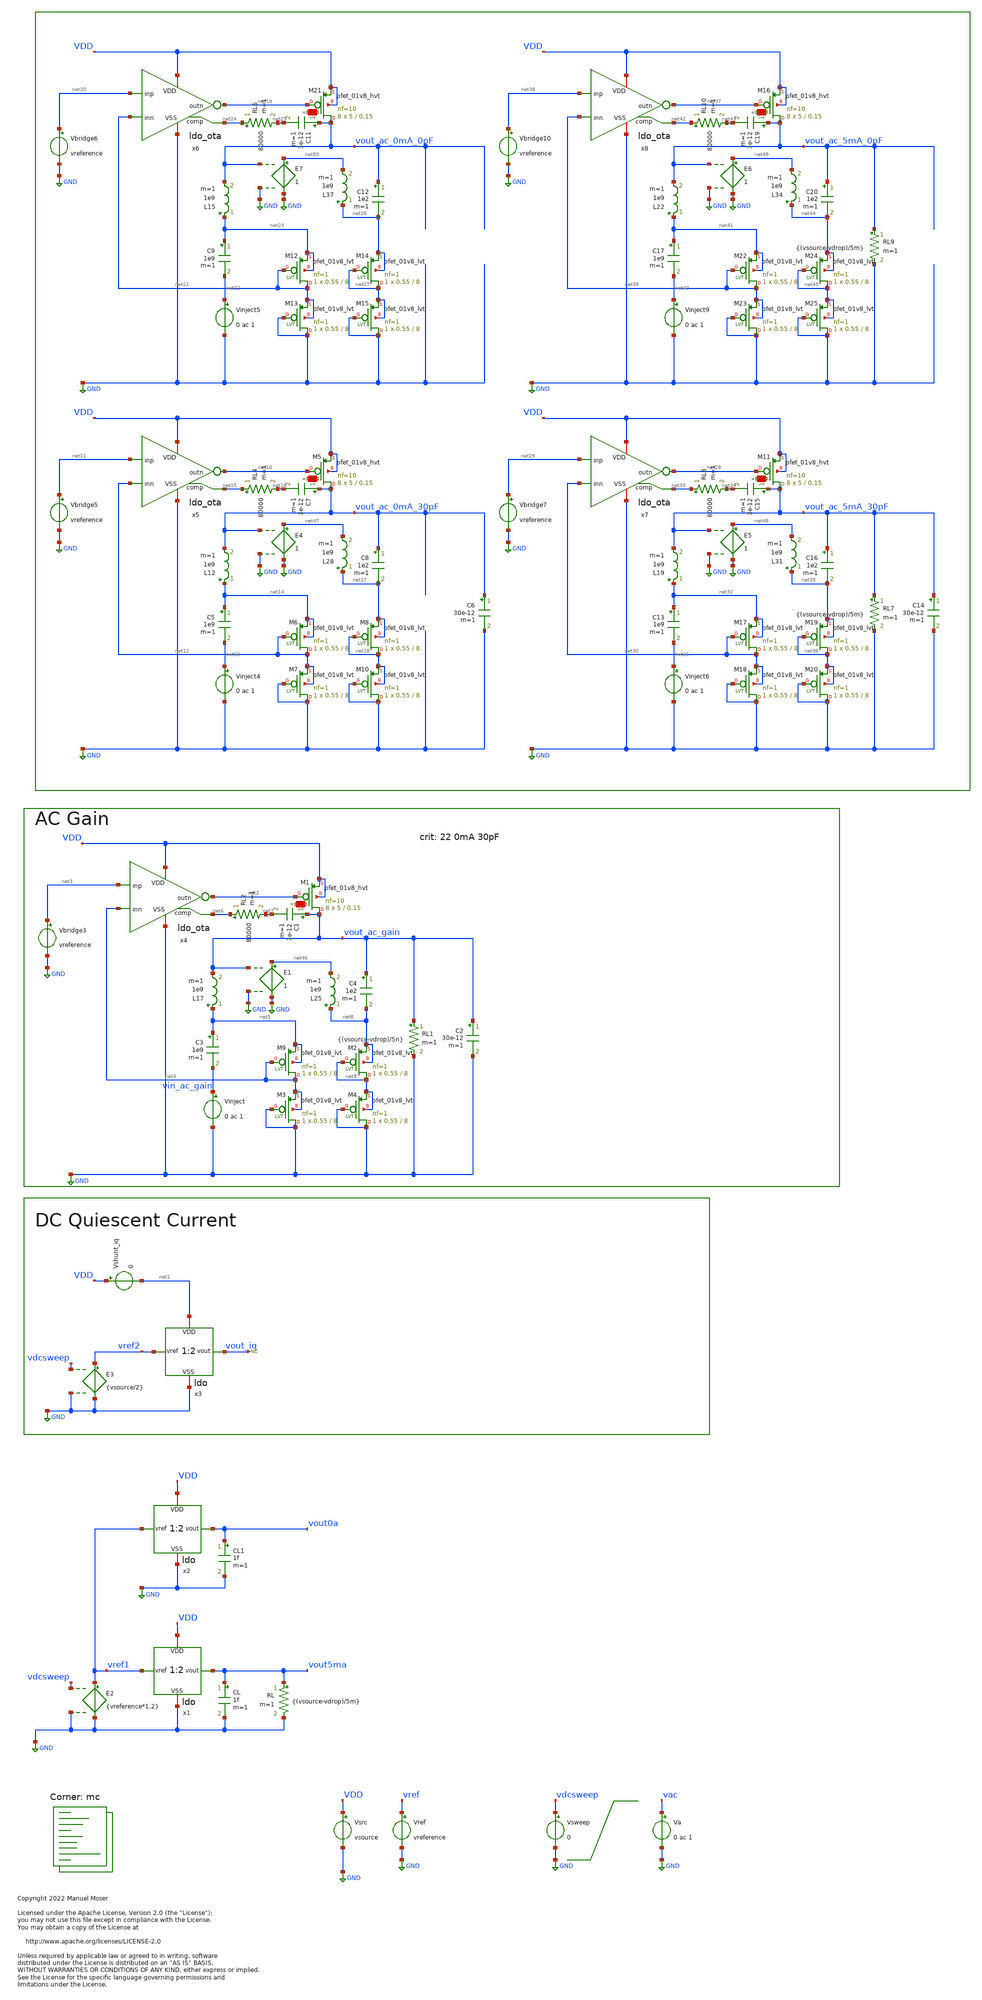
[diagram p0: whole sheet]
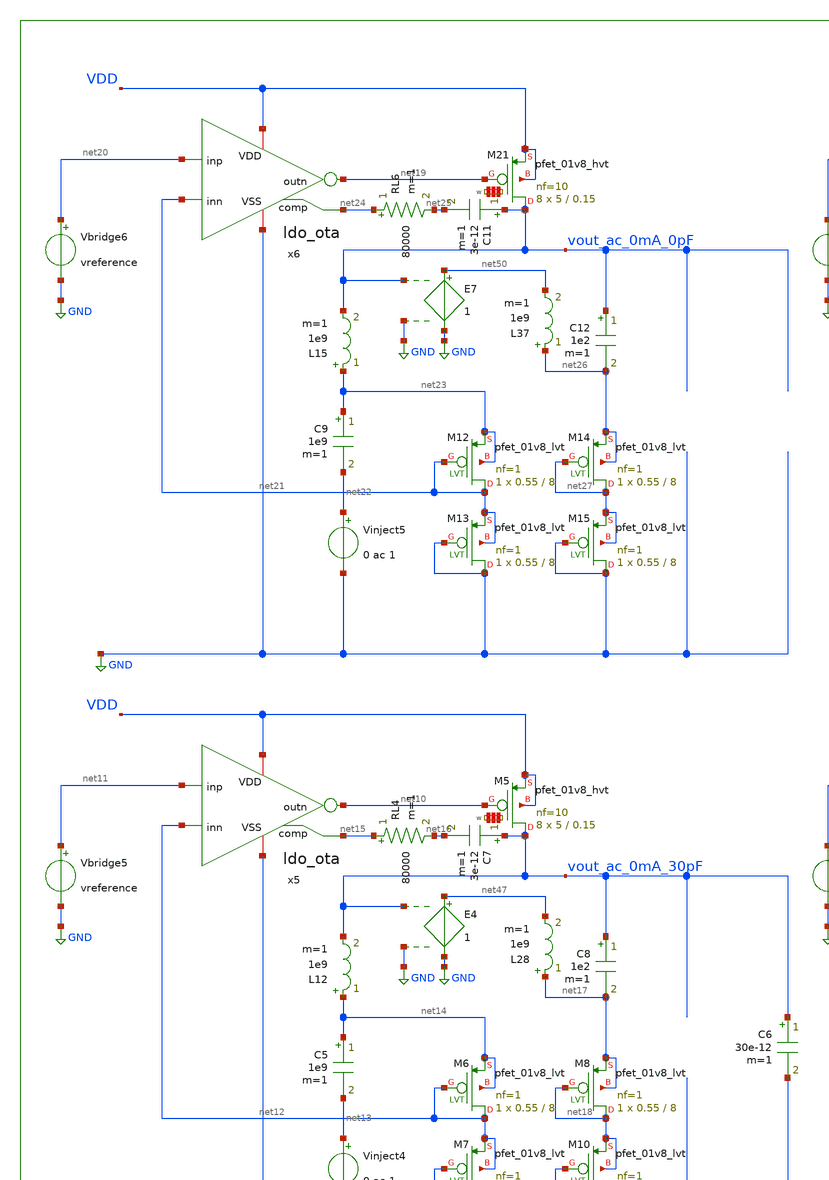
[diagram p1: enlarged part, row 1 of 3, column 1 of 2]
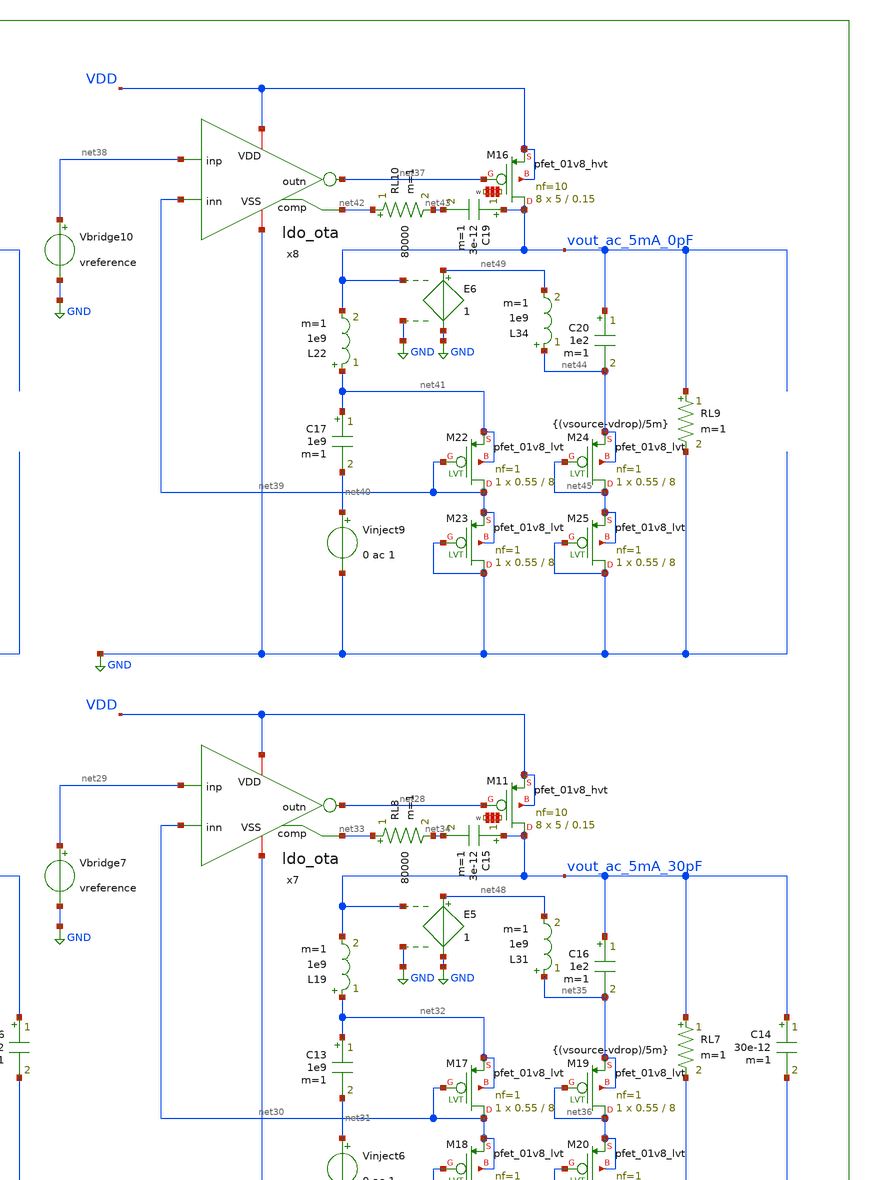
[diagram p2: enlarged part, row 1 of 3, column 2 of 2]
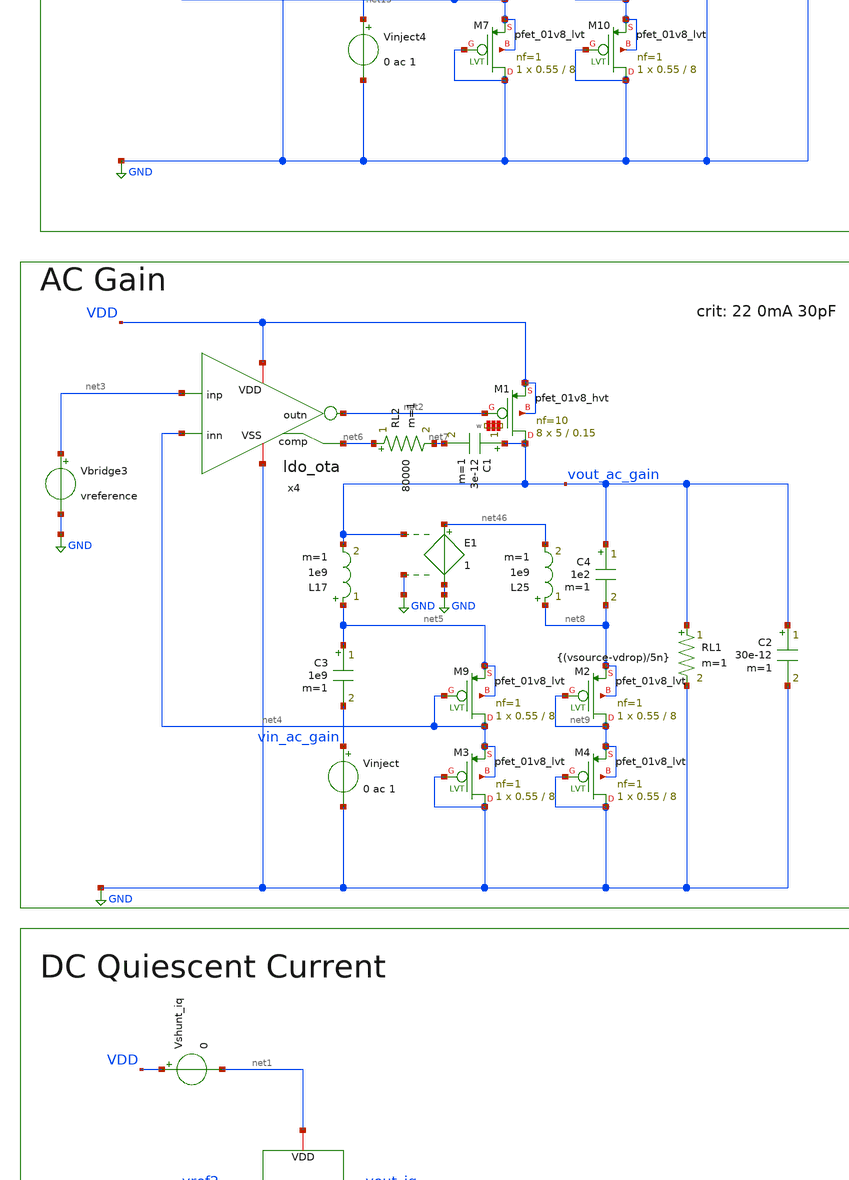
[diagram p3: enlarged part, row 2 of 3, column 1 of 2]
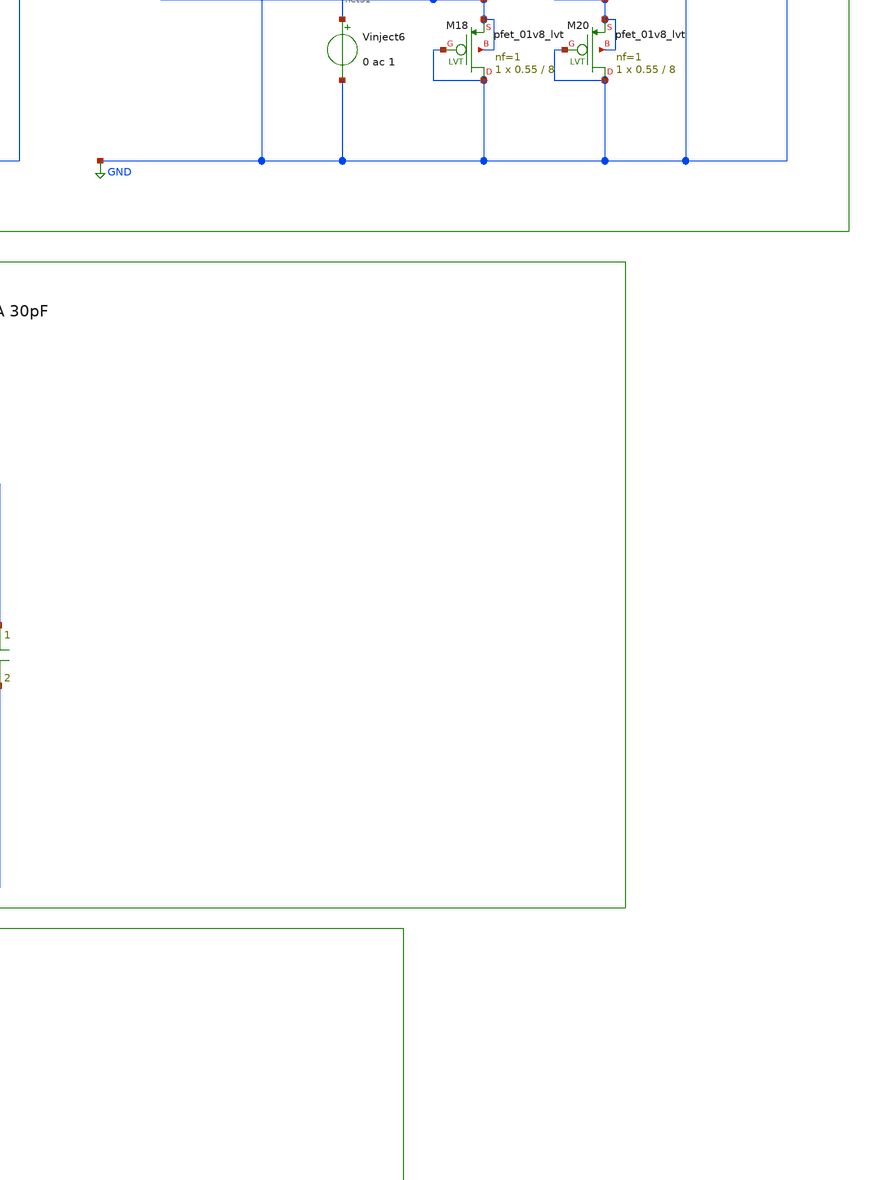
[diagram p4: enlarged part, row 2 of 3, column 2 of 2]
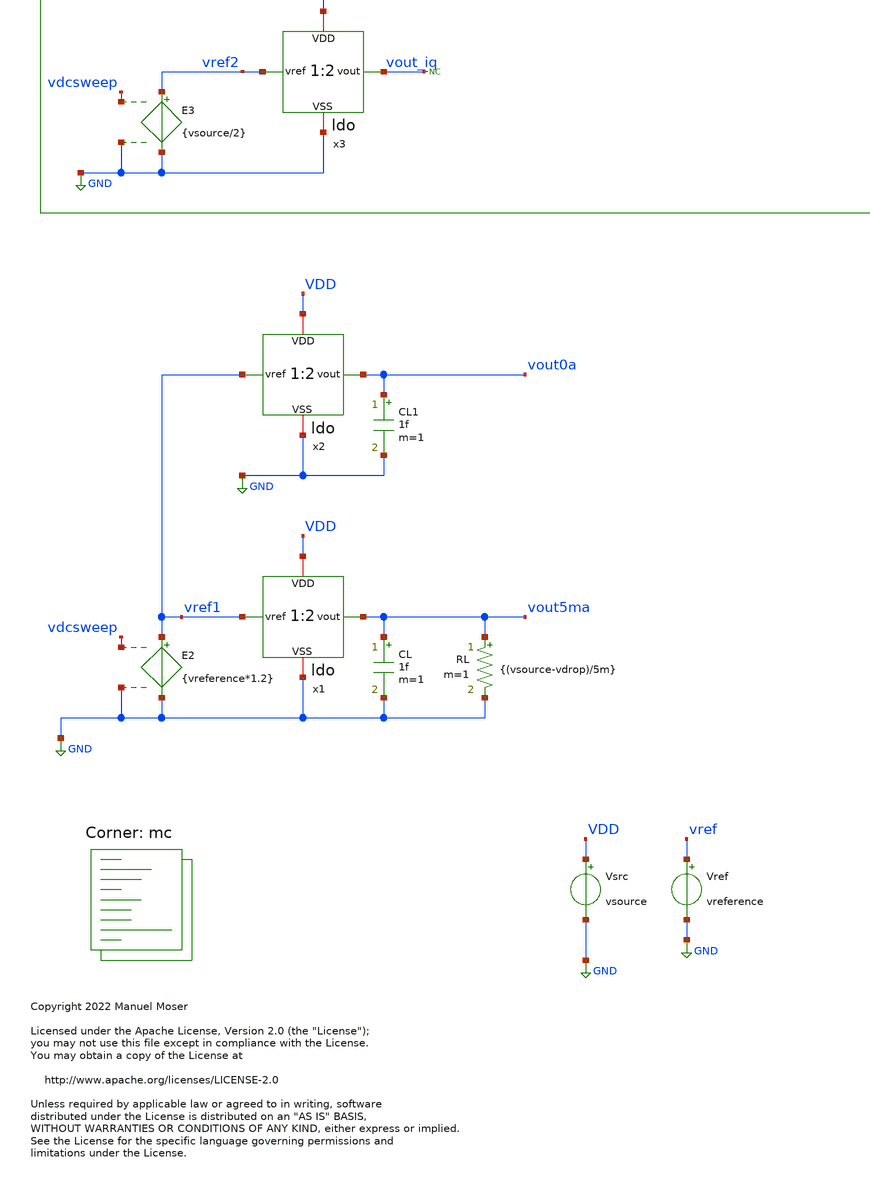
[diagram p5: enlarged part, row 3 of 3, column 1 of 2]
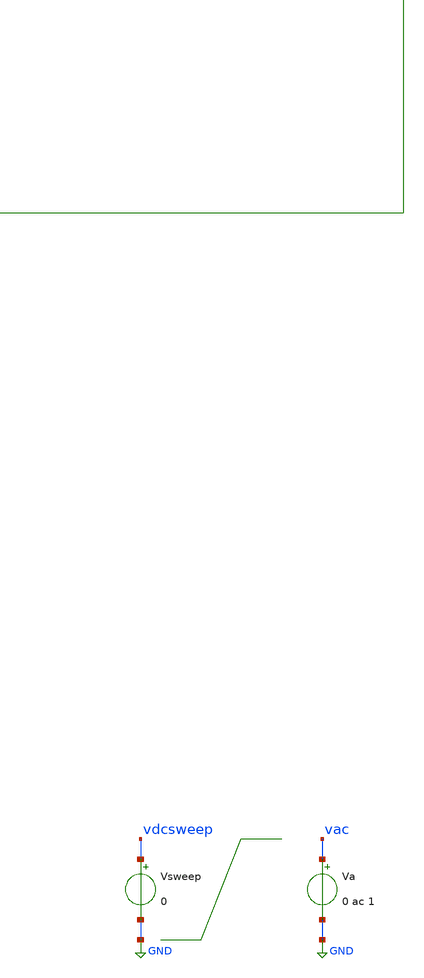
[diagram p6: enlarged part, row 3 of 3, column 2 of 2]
** sch_path: xschem/ldo_tb.sch
* Copyright 2022 Manuel Moser
* Licensed under the Apache License, Version 2.0 (the "License");
**.subckt ldo_tb
Vref vref GND vreference
Vsrc VDD GND vsource
Va vac GND 0 ac 1
CL vout5ma GND 1f m=1
RL vout5ma GND {(vsource-vdrop)/5m} m=1
x1 VDD vref1 vout5ma GND ldo
CL1 vout0a GND 1f m=1
x2 VDD vref1 vout0a GND ldo
Vsweep vdcsweep GND 0
E2 vref1 GND vdcsweep GND {vreference*1.2}
x3 net1 vref2 vout_iq GND ldo
Vshunt_iq VDD net1 0
E3 vref2 GND vdcsweep GND {vsource/2}
* noconn vout_iq
x4 VDD net3 net2 net4 GND net6 ldo_ota
L17 net5 vout_ac_gain 1e9 m=1
C3 net5 vin_ac_gain 1e9 m=1
Vinject vin_ac_gain GND 0 ac 1
Vbridge3 net3 GND vreference
RL1 vout_ac_gain GND {(vsource-vdrop)/5n} m=1
C2 vout_ac_gain GND 30e-12 m=1
C1 vout_ac_gain net7 3e-12 m=1
RL2 net6 net7 80000 m=1
XM9 net4 net4 net5 net5 sky130_fd_pr__pfet_01v8_lvt L=8 W=0.55 nf=1 ad='int((nf+1)/2) * W/nf * 0.29'
+ as='int((nf+2)/2) * W/nf * 0.29' pd='2*int((nf+1)/2) * (W/nf + 0.29)' ps='2*int((nf+2)/2) * (W/nf + 0.29)'
+ nrd='0.29 / W' nrs='0.29 / W' sa=0 sb=0 sd=0 mult=1 m=1
XM3 GND GND net4 net4 sky130_fd_pr__pfet_01v8_lvt L=8 W=0.55 nf=1 ad='int((nf+1)/2) * W/nf * 0.29' as='int((nf+2)/2) * W/nf * 0.29'
+ pd='2*int((nf+1)/2) * (W/nf + 0.29)' ps='2*int((nf+2)/2) * (W/nf + 0.29)' nrd='0.29 / W' nrs='0.29 / W'
+ sa=0 sb=0 sd=0 mult=1 m=1
XM2 net9 net9 net8 net8 sky130_fd_pr__pfet_01v8_lvt L=8 W=0.55 nf=1 ad='int((nf+1)/2) * W/nf * 0.29'
+ as='int((nf+2)/2) * W/nf * 0.29' pd='2*int((nf+1)/2) * (W/nf + 0.29)' ps='2*int((nf+2)/2) * (W/nf + 0.29)'
+ nrd='0.29 / W' nrs='0.29 / W' sa=0 sb=0 sd=0 mult=1 m=1
XM4 GND GND net9 net9 sky130_fd_pr__pfet_01v8_lvt L=8 W=0.55 nf=1 ad='int((nf+1)/2) * W/nf * 0.29' as='int((nf+2)/2) * W/nf * 0.29'
+ pd='2*int((nf+1)/2) * (W/nf + 0.29)' ps='2*int((nf+2)/2) * (W/nf + 0.29)' nrd='0.29 / W' nrs='0.29 / W'
+ sa=0 sb=0 sd=0 mult=1 m=1
C4 vout_ac_gain net8 1e2 m=1
x5 VDD net11 net10 net12 GND net15 ldo_ota
L12 net14 vout_ac_0mA_30pF 1e9 m=1
C5 net14 net13 1e9 m=1
Vinject4 net13 GND 0 ac 1
Vbridge5 net11 GND vreference
C6 vout_ac_0mA_30pF GND 30e-12 m=1
C7 vout_ac_0mA_30pF net16 3e-12 m=1
RL4 net15 net16 80000 m=1
XM6 net12 net12 net14 net14 sky130_fd_pr__pfet_01v8_lvt L=8 W=0.55 nf=1 ad='int((nf+1)/2) * W/nf * 0.29'
+ as='int((nf+2)/2) * W/nf * 0.29' pd='2*int((nf+1)/2) * (W/nf + 0.29)' ps='2*int((nf+2)/2) * (W/nf + 0.29)'
+ nrd='0.29 / W' nrs='0.29 / W' sa=0 sb=0 sd=0 mult=1 m=1
XM7 GND GND net12 net12 sky130_fd_pr__pfet_01v8_lvt L=8 W=0.55 nf=1 ad='int((nf+1)/2) * W/nf * 0.29'
+ as='int((nf+2)/2) * W/nf * 0.29' pd='2*int((nf+1)/2) * (W/nf + 0.29)' ps='2*int((nf+2)/2) * (W/nf + 0.29)'
+ nrd='0.29 / W' nrs='0.29 / W' sa=0 sb=0 sd=0 mult=1 m=1
XM8 net18 net18 net17 net17 sky130_fd_pr__pfet_01v8_lvt L=8 W=0.55 nf=1 ad='int((nf+1)/2) * W/nf * 0.29'
+ as='int((nf+2)/2) * W/nf * 0.29' pd='2*int((nf+1)/2) * (W/nf + 0.29)' ps='2*int((nf+2)/2) * (W/nf + 0.29)'
+ nrd='0.29 / W' nrs='0.29 / W' sa=0 sb=0 sd=0 mult=1 m=1
XM10 GND GND net18 net18 sky130_fd_pr__pfet_01v8_lvt L=8 W=0.55 nf=1 ad='int((nf+1)/2) * W/nf * 0.29'
+ as='int((nf+2)/2) * W/nf * 0.29' pd='2*int((nf+1)/2) * (W/nf + 0.29)' ps='2*int((nf+2)/2) * (W/nf + 0.29)'
+ nrd='0.29 / W' nrs='0.29 / W' sa=0 sb=0 sd=0 mult=1 m=1
C8 vout_ac_0mA_30pF net17 1e2 m=1
x6 VDD net20 net19 net21 GND net24 ldo_ota
L15 net23 vout_ac_0mA_0pF 1e9 m=1
C9 net23 net22 1e9 m=1
Vinject5 net22 GND 0 ac 1
Vbridge6 net20 GND vreference
C11 vout_ac_0mA_0pF net25 3e-12 m=1
RL6 net24 net25 80000 m=1
XM12 net21 net21 net23 net23 sky130_fd_pr__pfet_01v8_lvt L=8 W=0.55 nf=1 ad='int((nf+1)/2) * W/nf * 0.29'
+ as='int((nf+2)/2) * W/nf * 0.29' pd='2*int((nf+1)/2) * (W/nf + 0.29)' ps='2*int((nf+2)/2) * (W/nf + 0.29)'
+ nrd='0.29 / W' nrs='0.29 / W' sa=0 sb=0 sd=0 mult=1 m=1
XM13 GND GND net21 net21 sky130_fd_pr__pfet_01v8_lvt L=8 W=0.55 nf=1 ad='int((nf+1)/2) * W/nf * 0.29'
+ as='int((nf+2)/2) * W/nf * 0.29' pd='2*int((nf+1)/2) * (W/nf + 0.29)' ps='2*int((nf+2)/2) * (W/nf + 0.29)'
+ nrd='0.29 / W' nrs='0.29 / W' sa=0 sb=0 sd=0 mult=1 m=1
XM14 net27 net27 net26 net26 sky130_fd_pr__pfet_01v8_lvt L=8 W=0.55 nf=1 ad='int((nf+1)/2) * W/nf * 0.29'
+ as='int((nf+2)/2) * W/nf * 0.29' pd='2*int((nf+1)/2) * (W/nf + 0.29)' ps='2*int((nf+2)/2) * (W/nf + 0.29)'
+ nrd='0.29 / W' nrs='0.29 / W' sa=0 sb=0 sd=0 mult=1 m=1
XM15 GND GND net27 net27 sky130_fd_pr__pfet_01v8_lvt L=8 W=0.55 nf=1 ad='int((nf+1)/2) * W/nf * 0.29'
+ as='int((nf+2)/2) * W/nf * 0.29' pd='2*int((nf+1)/2) * (W/nf + 0.29)' ps='2*int((nf+2)/2) * (W/nf + 0.29)'
+ nrd='0.29 / W' nrs='0.29 / W' sa=0 sb=0 sd=0 mult=1 m=1
C12 vout_ac_0mA_0pF net26 1e2 m=1
x7 VDD net29 net28 net30 GND net33 ldo_ota
L19 net32 vout_ac_5mA_30pF 1e9 m=1
C13 net32 net31 1e9 m=1
Vinject6 net31 GND 0 ac 1
Vbridge7 net29 GND vreference
RL7 vout_ac_5mA_30pF GND {(vsource-vdrop)/5m} m=1
C14 vout_ac_5mA_30pF GND 30e-12 m=1
C15 vout_ac_5mA_30pF net34 3e-12 m=1
RL8 net33 net34 80000 m=1
XM17 net30 net30 net32 net32 sky130_fd_pr__pfet_01v8_lvt L=8 W=0.55 nf=1 ad='int((nf+1)/2) * W/nf * 0.29'
+ as='int((nf+2)/2) * W/nf * 0.29' pd='2*int((nf+1)/2) * (W/nf + 0.29)' ps='2*int((nf+2)/2) * (W/nf + 0.29)'
+ nrd='0.29 / W' nrs='0.29 / W' sa=0 sb=0 sd=0 mult=1 m=1
XM18 GND GND net30 net30 sky130_fd_pr__pfet_01v8_lvt L=8 W=0.55 nf=1 ad='int((nf+1)/2) * W/nf * 0.29'
+ as='int((nf+2)/2) * W/nf * 0.29' pd='2*int((nf+1)/2) * (W/nf + 0.29)' ps='2*int((nf+2)/2) * (W/nf + 0.29)'
+ nrd='0.29 / W' nrs='0.29 / W' sa=0 sb=0 sd=0 mult=1 m=1
XM19 net36 net36 net35 net35 sky130_fd_pr__pfet_01v8_lvt L=8 W=0.55 nf=1 ad='int((nf+1)/2) * W/nf * 0.29'
+ as='int((nf+2)/2) * W/nf * 0.29' pd='2*int((nf+1)/2) * (W/nf + 0.29)' ps='2*int((nf+2)/2) * (W/nf + 0.29)'
+ nrd='0.29 / W' nrs='0.29 / W' sa=0 sb=0 sd=0 mult=1 m=1
XM20 GND GND net36 net36 sky130_fd_pr__pfet_01v8_lvt L=8 W=0.55 nf=1 ad='int((nf+1)/2) * W/nf * 0.29'
+ as='int((nf+2)/2) * W/nf * 0.29' pd='2*int((nf+1)/2) * (W/nf + 0.29)' ps='2*int((nf+2)/2) * (W/nf + 0.29)'
+ nrd='0.29 / W' nrs='0.29 / W' sa=0 sb=0 sd=0 mult=1 m=1
C16 vout_ac_5mA_30pF net35 1e2 m=1
x8 VDD net38 net37 net39 GND net42 ldo_ota
L22 net41 vout_ac_5mA_0pF 1e9 m=1
C17 net41 net40 1e9 m=1
Vinject9 net40 GND 0 ac 1
Vbridge10 net38 GND vreference
RL9 vout_ac_5mA_0pF GND {(vsource-vdrop)/5m} m=1
C19 vout_ac_5mA_0pF net43 3e-12 m=1
RL10 net42 net43 80000 m=1
XM22 net39 net39 net41 net41 sky130_fd_pr__pfet_01v8_lvt L=8 W=0.55 nf=1 ad='int((nf+1)/2) * W/nf * 0.29'
+ as='int((nf+2)/2) * W/nf * 0.29' pd='2*int((nf+1)/2) * (W/nf + 0.29)' ps='2*int((nf+2)/2) * (W/nf + 0.29)'
+ nrd='0.29 / W' nrs='0.29 / W' sa=0 sb=0 sd=0 mult=1 m=1
XM23 GND GND net39 net39 sky130_fd_pr__pfet_01v8_lvt L=8 W=0.55 nf=1 ad='int((nf+1)/2) * W/nf * 0.29'
+ as='int((nf+2)/2) * W/nf * 0.29' pd='2*int((nf+1)/2) * (W/nf + 0.29)' ps='2*int((nf+2)/2) * (W/nf + 0.29)'
+ nrd='0.29 / W' nrs='0.29 / W' sa=0 sb=0 sd=0 mult=1 m=1
XM24 net45 net45 net44 net44 sky130_fd_pr__pfet_01v8_lvt L=8 W=0.55 nf=1 ad='int((nf+1)/2) * W/nf * 0.29'
+ as='int((nf+2)/2) * W/nf * 0.29' pd='2*int((nf+1)/2) * (W/nf + 0.29)' ps='2*int((nf+2)/2) * (W/nf + 0.29)'
+ nrd='0.29 / W' nrs='0.29 / W' sa=0 sb=0 sd=0 mult=1 m=1
XM25 GND GND net45 net45 sky130_fd_pr__pfet_01v8_lvt L=8 W=0.55 nf=1 ad='int((nf+1)/2) * W/nf * 0.29'
+ as='int((nf+2)/2) * W/nf * 0.29' pd='2*int((nf+1)/2) * (W/nf + 0.29)' ps='2*int((nf+2)/2) * (W/nf + 0.29)'
+ nrd='0.29 / W' nrs='0.29 / W' sa=0 sb=0 sd=0 mult=1 m=1
C20 vout_ac_5mA_0pF net44 1e2 m=1
L25 net8 net46 1e9 m=1
E1 net46 GND vout_ac_gain GND 1
L28 net17 net47 1e9 m=1
E4 net47 GND vout_ac_0mA_30pF GND 1
L31 net35 net48 1e9 m=1
E5 net48 GND vout_ac_5mA_30pF GND 1
L34 net44 net49 1e9 m=1
E6 net49 GND vout_ac_5mA_0pF GND 1
L37 net26 net50 1e9 m=1
E7 net50 GND vout_ac_0mA_0pF GND 1
XM1 vout_ac_gain net2 VDD VDD sky130_fd_pr__pfet_01v8_hvt L=0.15 W='5 * 10 ' nf=10 ad='int((nf+1)/2) * W / nf * 0.29'
+ as='int((nf+2)/2) * W / nf * 0.29' pd='2*int((nf+1)/2) * (W / nf + 0.29)' ps='2*int((nf+2)/2) * (W / nf + 0.29)'
+ nrd='0.29 / W ' nrs='0.29 / W ' sa=0 sb=0 sd=0 mult=8 m=8
XM5 vout_ac_0mA_30pF net10 VDD VDD sky130_fd_pr__pfet_01v8_hvt L=0.15 W='5 * 10 ' nf=10 ad='int((nf+1)/2) * W / nf * 0.29'
+ as='int((nf+2)/2) * W / nf * 0.29' pd='2*int((nf+1)/2) * (W / nf + 0.29)' ps='2*int((nf+2)/2) * (W / nf + 0.29)'
+ nrd='0.29 / W ' nrs='0.29 / W ' sa=0 sb=0 sd=0 mult=8 m=8
XM11 vout_ac_5mA_30pF net28 VDD VDD sky130_fd_pr__pfet_01v8_hvt L=0.15 W='5 * 10 ' nf=10 ad='int((nf+1)/2) * W / nf * 0.29'
+ as='int((nf+2)/2) * W / nf * 0.29' pd='2*int((nf+1)/2) * (W / nf + 0.29)' ps='2*int((nf+2)/2) * (W / nf + 0.29)'
+ nrd='0.29 / W ' nrs='0.29 / W ' sa=0 sb=0 sd=0 mult=8 m=8
XM16 vout_ac_5mA_0pF net37 VDD VDD sky130_fd_pr__pfet_01v8_hvt L=0.15 W='5 * 10 ' nf=10 ad='int((nf+1)/2) * W / nf * 0.29'
+ as='int((nf+2)/2) * W / nf * 0.29' pd='2*int((nf+1)/2) * (W / nf + 0.29)' ps='2*int((nf+2)/2) * (W / nf + 0.29)'
+ nrd='0.29 / W ' nrs='0.29 / W ' sa=0 sb=0 sd=0 mult=8 m=8
XM21 vout_ac_0mA_0pF net19 VDD VDD sky130_fd_pr__pfet_01v8_hvt L=0.15 W='5 * 10 ' nf=10 ad='int((nf+1)/2) * W / nf * 0.29'
+ as='int((nf+2)/2) * W / nf * 0.29' pd='2*int((nf+1)/2) * (W / nf + 0.29)' ps='2*int((nf+2)/2) * (W / nf + 0.29)'
+ nrd='0.29 / W ' nrs='0.29 / W ' sa=0 sb=0 sd=0 mult=8 m=8
**** begin user architecture code



.temp 27
*.option gmin = 1e-16
.option RSHUNT=1E15
.option method = gear

.param vsource = 1.80
.param vdrop = 0.20
.param vreference = {(vsource-vdrop)/2}

.save all
.options savecurrents

.control
set num_threads = 12
write results_ldo.raw
set appendwrite

repeat 10
reset

dc vsweep 0 1 0.01 temp -30 60 90
*dc vsweep 0 1 0.01
write results_ldo.raw   vref1 vout5ma vout0a x1.vota x1.vfb
+ @m.x1.xm9.msky130_fd_pr__pfet_01v8_lvt[id]  vref2 i(vshunt_iq) vout_ac_gain

ac dec 10 1 10meg
write results_ldo.raw vout_ac_0mA_0pF vout_ac_0mA_30pF vout_ac_5mA_0pF vout_ac_5mA_30pF

*pz vinject gnd vout_ac_gain gnd vol pz


end

.endc




.lib $::SKYWATER_MODELS/sky130.lib.spice mc
**** end user architecture code
**.ends

* expanding   symbol:  ldo.sym # of pins=4
** sym_path: xschem/ldo.sym
** sch_path: xschem/ldo.sch
.subckt ldo VDD vref vout VSS
*.ipin vref
*.iopin VDD
*.iopin VSS
*.opin vout
x1 VDD vref vota vfb VSS net1 ldo_ota
XM1 vout vota VDD VDD sky130_fd_pr__pfet_01v8 L=0.15 W='5 * 5 ' nf=5 ad='int((nf+1)/2) * W / nf * 0.29'
+ as='int((nf+2)/2) * W / nf * 0.29' pd='2*int((nf+1)/2) * (W / nf + 0.29)' ps='2*int((nf+2)/2) * (W / nf + 0.29)'
+ nrd='0.29 / W ' nrs='0.29 / W ' sa=0 sb=0 sd=0 mult=14 m=14
C1 vout net2 3e-12 m=1
RL2 net1 net2 80000 m=1
XM9 vfb vfb vout vout sky130_fd_pr__pfet_01v8_lvt L=8 W=0.55 nf=1 ad='int((nf+1)/2) * W/nf * 0.29' as='int((nf+2)/2) * W/nf * 0.29'
+ pd='2*int((nf+1)/2) * (W/nf + 0.29)' ps='2*int((nf+2)/2) * (W/nf + 0.29)' nrd='0.29 / W' nrs='0.29 / W'
+ sa=0 sb=0 sd=0 mult=1 m=1
XM3 VSS VSS vfb vfb sky130_fd_pr__pfet_01v8_lvt L=8 W=0.55 nf=1 ad='int((nf+1)/2) * W/nf * 0.29' as='int((nf+2)/2) * W/nf * 0.29'
+ pd='2*int((nf+1)/2) * (W/nf + 0.29)' ps='2*int((nf+2)/2) * (W/nf + 0.29)' nrd='0.29 / W' nrs='0.29 / W'
+ sa=0 sb=0 sd=0 mult=1 m=1
.ends


* expanding   symbol:  ldo_ota.sym # of pins=6
** sym_path: xschem/ldo_ota.sym
** sch_path: xschem/ldo_ota.sch
.subckt ldo_ota VDD inp outn inn VSS comp
*.iopin VDD
*.iopin VSS
*.ipin inp
*.ipin inn
*.opin outn
*.opin comp
x2 bias2 VDD VSS bias1 ldo_isource
XM10 net1 bias2 VDD VDD sky130_fd_pr__pfet_01v8_lvt L=8 W='0.55 * 1 ' nf=1 ad='int((nf+1)/2) * W / nf * 0.29'
+ as='int((nf+2)/2) * W / nf * 0.29' pd='2*int((nf+1)/2) * (W / nf + 0.29)' ps='2*int((nf+2)/2) * (W / nf + 0.29)'
+ nrd='0.29 / W ' nrs='0.29 / W ' sa=0 sb=0 sd=0 mult=1 m=1
XM12 bias2 bias2 net1 VDD sky130_fd_pr__pfet_01v8_lvt L=1 W='3 * 3 ' nf=3 ad='int((nf+1)/2) * W / nf * 0.29'
+ as='int((nf+2)/2) * W / nf * 0.29' pd='2*int((nf+1)/2) * (W / nf + 0.29)' ps='2*int((nf+2)/2) * (W / nf + 0.29)'
+ nrd='0.29 / W ' nrs='0.29 / W ' sa=0 sb=0 sd=0 mult=1 m=1
XM1 net2 bias1 VDD VDD sky130_fd_pr__pfet_01v8_lvt L=8 W='0.55 * 4 ' nf=4 ad='int((nf+1)/2) * W / nf * 0.29'
+ as='int((nf+2)/2) * W / nf * 0.29' pd='2*int((nf+1)/2) * (W / nf + 0.29)' ps='2*int((nf+2)/2) * (W / nf + 0.29)'
+ nrd='0.29 / W ' nrs='0.29 / W ' sa=0 sb=0 sd=0 mult=1 m=1
XM2 bias1 bias2 net2 VDD sky130_fd_pr__pfet_01v8_lvt L=1 W='3 * 3 ' nf=3 ad='int((nf+1)/2) * W / nf * 0.29'
+ as='int((nf+2)/2) * W / nf * 0.29' pd='2*int((nf+1)/2) * (W / nf + 0.29)' ps='2*int((nf+2)/2) * (W / nf + 0.29)'
+ nrd='0.29 / W ' nrs='0.29 / W ' sa=0 sb=0 sd=0 mult=1 m=1
XM3 net3 bias1 VDD VDD sky130_fd_pr__pfet_01v8_lvt L=8 W='0.55 * 4 ' nf=4 ad='int((nf+1)/2) * W / nf * 0.29'
+ as='int((nf+2)/2) * W / nf * 0.29' pd='2*int((nf+1)/2) * (W / nf + 0.29)' ps='2*int((nf+2)/2) * (W / nf + 0.29)'
+ nrd='0.29 / W ' nrs='0.29 / W ' sa=0 sb=0 sd=0 mult=1 m=1
XM4 bias3 bias2 net3 VDD sky130_fd_pr__pfet_01v8_lvt L=1 W='3 * 3 ' nf=3 ad='int((nf+1)/2) * W / nf * 0.29'
+ as='int((nf+2)/2) * W / nf * 0.29' pd='2*int((nf+1)/2) * (W / nf + 0.29)' ps='2*int((nf+2)/2) * (W / nf + 0.29)'
+ nrd='0.29 / W ' nrs='0.29 / W ' sa=0 sb=0 sd=0 mult=1 m=1
XM5 net4 bias1 VDD VDD sky130_fd_pr__pfet_01v8_lvt L=8 W='0.55 * 4 ' nf=4 ad='int((nf+1)/2) * W / nf * 0.29'
+ as='int((nf+2)/2) * W / nf * 0.29' pd='2*int((nf+1)/2) * (W / nf + 0.29)' ps='2*int((nf+2)/2) * (W / nf + 0.29)'
+ nrd='0.29 / W ' nrs='0.29 / W ' sa=0 sb=0 sd=0 mult=1 m=1
XM8 bias4 bias2 net4 VDD sky130_fd_pr__pfet_01v8_lvt L=1 W='3 * 3 ' nf=3 ad='int((nf+1)/2) * W / nf * 0.29'
+ as='int((nf+2)/2) * W / nf * 0.29' pd='2*int((nf+1)/2) * (W / nf + 0.29)' ps='2*int((nf+2)/2) * (W / nf + 0.29)'
+ nrd='0.29 / W ' nrs='0.29 / W ' sa=0 sb=0 sd=0 mult=1 m=1
XM9 bias3 bias3 net5 VSS sky130_fd_pr__nfet_01v8_lvt L=0.5 W='1 * 2 ' nf=2 ad='int((nf+1)/2) * W / nf * 0.29'
+ as='int((nf+2)/2) * W / nf * 0.29' pd='2*int((nf+1)/2) * (W / nf + 0.29)' ps='2*int((nf+2)/2) * (W / nf + 0.29)'
+ nrd='0.29 / W ' nrs='0.29 / W ' sa=0 sb=0 sd=0 mult=1 m=1
XM11 net5 bias3 net10 VSS sky130_fd_pr__nfet_01v8 L=8 W='0.42 * 1 ' nf=1 ad='int((nf+1)/2) * W / nf * 0.29'
+ as='int((nf+2)/2) * W / nf * 0.29' pd='2*int((nf+1)/2) * (W / nf + 0.29)' ps='2*int((nf+2)/2) * (W / nf + 0.29)'
+ nrd='0.29 / W ' nrs='0.29 / W ' sa=0 sb=0 sd=0 mult=1 m=1
XM13 bias4 bias3 net6 VSS sky130_fd_pr__nfet_01v8_lvt L=0.5 W='1 * 2 ' nf=2 ad='int((nf+1)/2) * W / nf * 0.29'
+ as='int((nf+2)/2) * W / nf * 0.29' pd='2*int((nf+1)/2) * (W / nf + 0.29)' ps='2*int((nf+2)/2) * (W / nf + 0.29)'
+ nrd='0.29 / W ' nrs='0.29 / W ' sa=0 sb=0 sd=0 mult=1 m=1
XM14 net6 bias4 net7 VSS sky130_fd_pr__nfet_01v8 L=8 W='0.42 * 4 ' nf=4 ad='int((nf+1)/2) * W / nf * 0.29'
+ as='int((nf+2)/2) * W / nf * 0.29' pd='2*int((nf+1)/2) * (W / nf + 0.29)' ps='2*int((nf+2)/2) * (W / nf + 0.29)'
+ nrd='0.29 / W ' nrs='0.29 / W ' sa=0 sb=0 sd=0 mult=1 m=1
XM6 net7 bias4 net8 VSS sky130_fd_pr__nfet_01v8 L=8 W='0.42 * 4 ' nf=4 ad='int((nf+1)/2) * W / nf * 0.29'
+ as='int((nf+2)/2) * W / nf * 0.29' pd='2*int((nf+1)/2) * (W / nf + 0.29)' ps='2*int((nf+2)/2) * (W / nf + 0.29)'
+ nrd='0.29 / W ' nrs='0.29 / W ' sa=0 sb=0 sd=0 mult=1 m=1
XM7 net10 bias3 net9 VSS sky130_fd_pr__nfet_01v8 L=8 W='0.42 * 1 ' nf=1 ad='int((nf+1)/2) * W / nf * 0.29'
+ as='int((nf+2)/2) * W / nf * 0.29' pd='2*int((nf+1)/2) * (W / nf + 0.29)' ps='2*int((nf+2)/2) * (W / nf + 0.29)'
+ nrd='0.29 / W ' nrs='0.29 / W ' sa=0 sb=0 sd=0 mult=1 m=1
x1 VDD inp inn bias1 bias2 bias3 outn VSS bias4 comp ldo_fc_n
XM15 net9 bias3 net11 VSS sky130_fd_pr__nfet_01v8 L=8 W='0.42 * 1 ' nf=1 ad='int((nf+1)/2) * W / nf * 0.29'
+ as='int((nf+2)/2) * W / nf * 0.29' pd='2*int((nf+1)/2) * (W / nf + 0.29)' ps='2*int((nf+2)/2) * (W / nf + 0.29)'
+ nrd='0.29 / W ' nrs='0.29 / W ' sa=0 sb=0 sd=0 mult=1 m=1
XM16 net8 bias4 net12 VSS sky130_fd_pr__nfet_01v8 L=8 W='0.42 * 4 ' nf=4 ad='int((nf+1)/2) * W / nf * 0.29'
+ as='int((nf+2)/2) * W / nf * 0.29' pd='2*int((nf+1)/2) * (W / nf + 0.29)' ps='2*int((nf+2)/2) * (W / nf + 0.29)'
+ nrd='0.29 / W ' nrs='0.29 / W ' sa=0 sb=0 sd=0 mult=1 m=1
XM17 net12 bias4 VSS VSS sky130_fd_pr__nfet_01v8 L=8 W='0.42 * 4 ' nf=4 ad='int((nf+1)/2) * W / nf * 0.29'
+ as='int((nf+2)/2) * W / nf * 0.29' pd='2*int((nf+1)/2) * (W / nf + 0.29)' ps='2*int((nf+2)/2) * (W / nf + 0.29)'
+ nrd='0.29 / W ' nrs='0.29 / W ' sa=0 sb=0 sd=0 mult=1 m=1
XM18 net11 bias3 VSS VSS sky130_fd_pr__nfet_01v8 L=8 W='0.42 * 1 ' nf=1 ad='int((nf+1)/2) * W / nf * 0.29'
+ as='int((nf+2)/2) * W / nf * 0.29' pd='2*int((nf+1)/2) * (W / nf + 0.29)' ps='2*int((nf+2)/2) * (W / nf + 0.29)'
+ nrd='0.29 / W ' nrs='0.29 / W ' sa=0 sb=0 sd=0 mult=1 m=1
.ends


* expanding   symbol:  ldo_isource.sym # of pins=4
** sym_path: xschem/ldo_isource.sym
** sch_path: xschem/ldo_isource.sch
.subckt ldo_isource curr_n1 VDD VSS curr_n2
*.iopin VDD
*.iopin VSS
*.ipin curr_n1
*.ipin curr_n2
XMP2 VGP VGP net4 VDD sky130_fd_pr__pfet_01v8_lvt L=8 W='0.55 * 7 ' nf=7 ad='int((nf+1)/2) * W / nf * 0.29'
+ as='int((nf+2)/2) * W / nf * 0.29' pd='2*int((nf+1)/2) * (W / nf + 0.29)' ps='2*int((nf+2)/2) * (W / nf + 0.29)'
+ nrd='0.29 / W ' nrs='0.29 / W ' sa=0 sb=0 sd=0 mult=1 m=1
XMP1 VGN VGP net3 VDD sky130_fd_pr__pfet_01v8_lvt L=8 W='0.55 * 7 ' nf=7 ad='int((nf+1)/2) * W / nf * 0.29'
+ as='int((nf+2)/2) * W / nf * 0.29' pd='2*int((nf+1)/2) * (W / nf + 0.29)' ps='2*int((nf+2)/2) * (W / nf + 0.29)'
+ nrd='0.29 / W ' nrs='0.29 / W ' sa=0 sb=0 sd=0 mult=1 m=1
XMN1 VGN VGN net1 VSS sky130_fd_pr__nfet_01v8_lvt L=8 W='7 * 1 ' nf=1 ad='int((nf+1)/2) * W / nf * 0.29'
+ as='int((nf+2)/2) * W / nf * 0.29' pd='2*int((nf+1)/2) * (W / nf + 0.29)' ps='2*int((nf+2)/2) * (W / nf + 0.29)'
+ nrd='0.29 / W ' nrs='0.29 / W ' sa=0 sb=0 sd=0 mult=1 m=1
XMN2 VGP VGN net2 VSS sky130_fd_pr__nfet_01v8_lvt L=8 W='7 * 1 ' nf=1 ad='int((nf+1)/2) * W / nf * 0.29'
+ as='int((nf+2)/2) * W / nf * 0.29' pd='2*int((nf+1)/2) * (W / nf + 0.29)' ps='2*int((nf+2)/2) * (W / nf + 0.29)'
+ nrd='0.29 / W ' nrs='0.29 / W ' sa=0 sb=0 sd=0 mult=5 m=5
XMN3 net1 VGN VSS VSS sky130_fd_pr__nfet_01v8_lvt L=8 W='7 * 1 ' nf=1 ad='int((nf+1)/2) * W / nf * 0.29'
+ as='int((nf+2)/2) * W / nf * 0.29' pd='2*int((nf+1)/2) * (W / nf + 0.29)' ps='2*int((nf+2)/2) * (W / nf + 0.29)'
+ nrd='0.29 / W ' nrs='0.29 / W ' sa=0 sb=0 sd=0 mult=1 m=1
XMN4 net2 VGN Vref VSS sky130_fd_pr__nfet_01v8_lvt L=8 W='7 * 1 ' nf=1 ad='int((nf+1)/2) * W / nf * 0.29'
+ as='int((nf+2)/2) * W / nf * 0.29' pd='2*int((nf+1)/2) * (W / nf + 0.29)' ps='2*int((nf+2)/2) * (W / nf + 0.29)'
+ nrd='0.29 / W ' nrs='0.29 / W ' sa=0 sb=0 sd=0 mult=5 m=5
XMP4 net3 VGP VDD VDD sky130_fd_pr__pfet_01v8_lvt L=8 W='0.55 * 7 ' nf=7 ad='int((nf+1)/2) * W / nf * 0.29'
+ as='int((nf+2)/2) * W / nf * 0.29' pd='2*int((nf+1)/2) * (W / nf + 0.29)' ps='2*int((nf+2)/2) * (W / nf + 0.29)'
+ nrd='0.29 / W ' nrs='0.29 / W ' sa=0 sb=0 sd=0 mult=1 m=1
XMP5 net4 VGP VDD VDD sky130_fd_pr__pfet_01v8_lvt L=8 W='0.55 * 7 ' nf=7 ad='int((nf+1)/2) * W / nf * 0.29'
+ as='int((nf+2)/2) * W / nf * 0.29' pd='2*int((nf+1)/2) * (W / nf + 0.29)' ps='2*int((nf+2)/2) * (W / nf + 0.29)'
+ nrd='0.29 / W ' nrs='0.29 / W ' sa=0 sb=0 sd=0 mult=1 m=1
XMP3 Vrefgate VGP net19 VDD sky130_fd_pr__pfet_01v8_lvt L=8 W='0.55 * 7 ' nf=7 ad='int((nf+1)/2) * W / nf * 0.29'
+ as='int((nf+2)/2) * W / nf * 0.29' pd='2*int((nf+1)/2) * (W / nf + 0.29)' ps='2*int((nf+2)/2) * (W / nf + 0.29)'
+ nrd='0.29 / W ' nrs='0.29 / W ' sa=0 sb=0 sd=0 mult=1 m=1
XM2 net5 Vrefgate net6 VSS sky130_fd_pr__nfet_01v8 L=4 W='1 * 1 ' nf=1 ad='int((nf+1)/2) * W / nf * 0.29'
+ as='int((nf+2)/2) * W / nf * 0.29' pd='2*int((nf+1)/2) * (W / nf + 0.29)' ps='2*int((nf+2)/2) * (W / nf + 0.29)'
+ nrd='0.29 / W ' nrs='0.29 / W ' sa=0 sb=0 sd=0 mult=1 m=1
XM3 net8 Vrefgate VSS VSS sky130_fd_pr__nfet_01v8 L=4 W='1 * 1 ' nf=1 ad='int((nf+1)/2) * W / nf * 0.29'
+ as='int((nf+2)/2) * W / nf * 0.29' pd='2*int((nf+1)/2) * (W / nf + 0.29)' ps='2*int((nf+2)/2) * (W / nf + 0.29)'
+ nrd='0.29 / W ' nrs='0.29 / W ' sa=0 sb=0 sd=0 mult=1 m=1
XM1 net7 Vrefgate net8 VSS sky130_fd_pr__nfet_01v8 L=4 W='1 * 1 ' nf=1 ad='int((nf+1)/2) * W / nf * 0.29'
+ as='int((nf+2)/2) * W / nf * 0.29' pd='2*int((nf+1)/2) * (W / nf + 0.29)' ps='2*int((nf+2)/2) * (W / nf + 0.29)'
+ nrd='0.29 / W ' nrs='0.29 / W ' sa=0 sb=0 sd=0 mult=1 m=1
XM4 net6 Vrefgate net7 VSS sky130_fd_pr__nfet_01v8 L=4 W='1 * 1 ' nf=1 ad='int((nf+1)/2) * W / nf * 0.29'
+ as='int((nf+2)/2) * W / nf * 0.29' pd='2*int((nf+1)/2) * (W / nf + 0.29)' ps='2*int((nf+2)/2) * (W / nf + 0.29)'
+ nrd='0.29 / W ' nrs='0.29 / W ' sa=0 sb=0 sd=0 mult=1 m=1
XMN5 net10 Vrefgate VSS VSS sky130_fd_pr__nfet_01v8_lvt L=4 W='1 * 1 ' nf=1 ad='int((nf+1)/2) * W / nf * 0.29'
+ as='int((nf+2)/2) * W / nf * 0.29' pd='2*int((nf+1)/2) * (W / nf + 0.29)' ps='2*int((nf+2)/2) * (W / nf + 0.29)'
+ nrd='0.29 / W ' nrs='0.29 / W ' sa=0 sb=0 sd=0 mult=1 m=1
XMN6 net14 Vrefgate net9 VSS sky130_fd_pr__nfet_01v8_lvt L=4 W='1 * 1 ' nf=1 ad='int((nf+1)/2) * W / nf * 0.29'
+ as='int((nf+2)/2) * W / nf * 0.29' pd='2*int((nf+1)/2) * (W / nf + 0.29)' ps='2*int((nf+2)/2) * (W / nf + 0.29)'
+ nrd='0.29 / W ' nrs='0.29 / W ' sa=0 sb=0 sd=0 mult=1 m=1
XMN9 net16 Vrefgate net14 VSS sky130_fd_pr__nfet_01v8_lvt L=4 W='1 * 1 ' nf=1 ad='int((nf+1)/2) * W / nf * 0.29'
+ as='int((nf+2)/2) * W / nf * 0.29' pd='2*int((nf+1)/2) * (W / nf + 0.29)' ps='2*int((nf+2)/2) * (W / nf + 0.29)'
+ nrd='0.29 / W ' nrs='0.29 / W ' sa=0 sb=0 sd=0 mult=1 m=1
XM5 Vrefgate Vrefgate net5 VSS sky130_fd_pr__nfet_01v8 L=4 W='1 * 1 ' nf=1 ad='int((nf+1)/2) * W / nf * 0.29'
+ as='int((nf+2)/2) * W / nf * 0.29' pd='2*int((nf+1)/2) * (W / nf + 0.29)' ps='2*int((nf+2)/2) * (W / nf + 0.29)'
+ nrd='0.29 / W ' nrs='0.29 / W ' sa=0 sb=0 sd=0 mult=1 m=1
XMN10 net11 Vrefgate net10 VSS sky130_fd_pr__nfet_01v8_lvt L=4 W='1 * 1 ' nf=1 ad='int((nf+1)/2) * W / nf * 0.29'
+ as='int((nf+2)/2) * W / nf * 0.29' pd='2*int((nf+1)/2) * (W / nf + 0.29)' ps='2*int((nf+2)/2) * (W / nf + 0.29)'
+ nrd='0.29 / W ' nrs='0.29 / W ' sa=0 sb=0 sd=0 mult=1 m=1
XMN11 net12 Vrefgate net11 VSS sky130_fd_pr__nfet_01v8_lvt L=4 W='1 * 1 ' nf=1 ad='int((nf+1)/2) * W / nf * 0.29'
+ as='int((nf+2)/2) * W / nf * 0.29' pd='2*int((nf+1)/2) * (W / nf + 0.29)' ps='2*int((nf+2)/2) * (W / nf + 0.29)'
+ nrd='0.29 / W ' nrs='0.29 / W ' sa=0 sb=0 sd=0 mult=1 m=1
XMN12 net13 Vrefgate net12 VSS sky130_fd_pr__nfet_01v8_lvt L=4 W='1 * 1 ' nf=1 ad='int((nf+1)/2) * W / nf * 0.29'
+ as='int((nf+2)/2) * W / nf * 0.29' pd='2*int((nf+1)/2) * (W / nf + 0.29)' ps='2*int((nf+2)/2) * (W / nf + 0.29)'
+ nrd='0.29 / W ' nrs='0.29 / W ' sa=0 sb=0 sd=0 mult=1 m=1
XMN13 net9 Vrefgate net13 VSS sky130_fd_pr__nfet_01v8_lvt L=4 W='1 * 1 ' nf=1 ad='int((nf+1)/2) * W / nf * 0.29'
+ as='int((nf+2)/2) * W / nf * 0.29' pd='2*int((nf+1)/2) * (W / nf + 0.29)' ps='2*int((nf+2)/2) * (W / nf + 0.29)'
+ nrd='0.29 / W ' nrs='0.29 / W ' sa=0 sb=0 sd=0 mult=1 m=1
XMN7 net18 Vrefgate net15 VSS sky130_fd_pr__nfet_01v8_lvt L=4 W='1 * 1 ' nf=1 ad='int((nf+1)/2) * W / nf * 0.29'
+ as='int((nf+2)/2) * W / nf * 0.29' pd='2*int((nf+1)/2) * (W / nf + 0.29)' ps='2*int((nf+2)/2) * (W / nf + 0.29)'
+ nrd='0.29 / W ' nrs='0.29 / W ' sa=0 sb=0 sd=0 mult=1 m=1
XMN8 Vref Vrefgate net18 VSS sky130_fd_pr__nfet_01v8_lvt L=4 W='1 * 1 ' nf=1 ad='int((nf+1)/2) * W / nf * 0.29'
+ as='int((nf+2)/2) * W / nf * 0.29' pd='2*int((nf+1)/2) * (W / nf + 0.29)' ps='2*int((nf+2)/2) * (W / nf + 0.29)'
+ nrd='0.29 / W ' nrs='0.29 / W ' sa=0 sb=0 sd=0 mult=1 m=1
XMN14 net17 Vrefgate net16 VSS sky130_fd_pr__nfet_01v8_lvt L=4 W='1 * 1 ' nf=1 ad='int((nf+1)/2) * W / nf * 0.29'
+ as='int((nf+2)/2) * W / nf * 0.29' pd='2*int((nf+1)/2) * (W / nf + 0.29)' ps='2*int((nf+2)/2) * (W / nf + 0.29)'
+ nrd='0.29 / W ' nrs='0.29 / W ' sa=0 sb=0 sd=0 mult=1 m=1
XMN15 net15 Vrefgate net17 VSS sky130_fd_pr__nfet_01v8_lvt L=4 W='1 * 1 ' nf=1 ad='int((nf+1)/2) * W / nf * 0.29'
+ as='int((nf+2)/2) * W / nf * 0.29' pd='2*int((nf+1)/2) * (W / nf + 0.29)' ps='2*int((nf+2)/2) * (W / nf + 0.29)'
+ nrd='0.29 / W ' nrs='0.29 / W ' sa=0 sb=0 sd=0 mult=1 m=1
XMP6 net19 VGP VDD VDD sky130_fd_pr__pfet_01v8_lvt L=8 W='0.55 * 7 ' nf=7 ad='int((nf+1)/2) * W / nf * 0.29'
+ as='int((nf+2)/2) * W / nf * 0.29' pd='2*int((nf+1)/2) * (W / nf + 0.29)' ps='2*int((nf+2)/2) * (W / nf + 0.29)'
+ nrd='0.29 / W ' nrs='0.29 / W ' sa=0 sb=0 sd=0 mult=1 m=1
XMN16 curr_n1 VGN net20 VSS sky130_fd_pr__nfet_01v8_lvt L=8 W='7 * 1 ' nf=1 ad='int((nf+1)/2) * W / nf * 0.29'
+ as='int((nf+2)/2) * W / nf * 0.29' pd='2*int((nf+1)/2) * (W / nf + 0.29)' ps='2*int((nf+2)/2) * (W / nf + 0.29)'
+ nrd='0.29 / W ' nrs='0.29 / W ' sa=0 sb=0 sd=0 mult=1 m=1
XMN17 net20 VGN VSS VSS sky130_fd_pr__nfet_01v8_lvt L=8 W='7 * 1 ' nf=1 ad='int((nf+1)/2) * W / nf * 0.29'
+ as='int((nf+2)/2) * W / nf * 0.29' pd='2*int((nf+1)/2) * (W / nf + 0.29)' ps='2*int((nf+2)/2) * (W / nf + 0.29)'
+ nrd='0.29 / W ' nrs='0.29 / W ' sa=0 sb=0 sd=0 mult=1 m=1
XM6 VGP vstartup VGN VSS sky130_fd_pr__nfet_01v8 L=4 W='1 * 1 ' nf=1 ad='int((nf+1)/2) * W / nf * 0.29'
+ as='int((nf+2)/2) * W / nf * 0.29' pd='2*int((nf+1)/2) * (W / nf + 0.29)' ps='2*int((nf+2)/2) * (W / nf + 0.29)'
+ nrd='0.29 / W ' nrs='0.29 / W ' sa=0 sb=0 sd=0 mult=1 m=1
XM7 vstartup Vrefgate VSS VSS sky130_fd_pr__nfet_01v8 L=4 W='1 * 1 ' nf=1 ad='int((nf+1)/2) * W / nf * 0.29'
+ as='int((nf+2)/2) * W / nf * 0.29' pd='2*int((nf+1)/2) * (W / nf + 0.29)' ps='2*int((nf+2)/2) * (W / nf + 0.29)'
+ nrd='0.29 / W ' nrs='0.29 / W ' sa=0 sb=0 sd=0 mult=1 m=1
XMN18 curr_n2 VGN net21 VSS sky130_fd_pr__nfet_01v8_lvt L=8 W='7 * 1 ' nf=1 ad='int((nf+1)/2) * W / nf * 0.29'
+ as='int((nf+2)/2) * W / nf * 0.29' pd='2*int((nf+1)/2) * (W / nf + 0.29)' ps='2*int((nf+2)/2) * (W / nf + 0.29)'
+ nrd='0.29 / W ' nrs='0.29 / W ' sa=0 sb=0 sd=0 mult=1 m=1
XMN19 net21 VGN VSS VSS sky130_fd_pr__nfet_01v8_lvt L=8 W='7 * 1 ' nf=1 ad='int((nf+1)/2) * W / nf * 0.29'
+ as='int((nf+2)/2) * W / nf * 0.29' pd='2*int((nf+1)/2) * (W / nf + 0.29)' ps='2*int((nf+2)/2) * (W / nf + 0.29)'
+ nrd='0.29 / W ' nrs='0.29 / W ' sa=0 sb=0 sd=0 mult=1 m=1
XC1 VDD vstartup sky130_fd_pr__cap_mim_m3_2 W=4 L=4 MF=1 m=1
.ends


* expanding   symbol:  ldo_fc_n.sym # of pins=10
** sym_path: xschem/ldo_fc_n.sym
** sch_path: xschem/ldo_fc_n.sch
.subckt ldo_fc_n VDD inp inn bias1 bias2 bias3 outn VSS bias4 comp
*.iopin VSS
*.iopin VDD
*.ipin inp
*.ipin inn
*.ipin bias1
*.opin outn
*.ipin bias2
*.ipin bias3
*.ipin bias4
*.opin comp
XMN4 outn bias3 net1 VSS sky130_fd_pr__nfet_01v8_lvt L=0.5 W='1 * 2 ' nf=2 ad='int((nf+1)/2) * W / nf * 0.29'
+ as='int((nf+2)/2) * W / nf * 0.29' pd='2*int((nf+1)/2) * (W / nf + 0.29)' ps='2*int((nf+2)/2) * (W / nf + 0.29)'
+ nrd='0.29 / W ' nrs='0.29 / W ' sa=0 sb=0 sd=0 mult=11 m=11
XMN7 net1 net3 net7 VSS sky130_fd_pr__nfet_01v8 L=8 W='0.42 * 4 ' nf=4 ad='int((nf+1)/2) * W / nf * 0.29'
+ as='int((nf+2)/2) * W / nf * 0.29' pd='2*int((nf+1)/2) * (W / nf + 0.29)' ps='2*int((nf+2)/2) * (W / nf + 0.29)'
+ nrd='0.29 / W ' nrs='0.29 / W ' sa=0 sb=0 sd=0 mult=11 m=11
XMN3 net3 bias3 net2 VSS sky130_fd_pr__nfet_01v8_lvt L=0.5 W='1 * 2 ' nf=2 ad='int((nf+1)/2) * W / nf * 0.29'
+ as='int((nf+2)/2) * W / nf * 0.29' pd='2*int((nf+1)/2) * (W / nf + 0.29)' ps='2*int((nf+2)/2) * (W / nf + 0.29)'
+ nrd='0.29 / W ' nrs='0.29 / W ' sa=0 sb=0 sd=0 mult=11 m=11
XMN6 net2 net3 net6 VSS sky130_fd_pr__nfet_01v8 L=8 W='0.42 * 4 ' nf=4 ad='int((nf+1)/2) * W / nf * 0.29'
+ as='int((nf+2)/2) * W / nf * 0.29' pd='2*int((nf+1)/2) * (W / nf + 0.29)' ps='2*int((nf+2)/2) * (W / nf + 0.29)'
+ nrd='0.29 / W ' nrs='0.29 / W ' sa=0 sb=0 sd=0 mult=11 m=11
XMP4 outn bias2 comp VDD sky130_fd_pr__pfet_01v8_lvt L=1 W='3 * 3 ' nf=3 ad='int((nf+1)/2) * W / nf * 0.29'
+ as='int((nf+2)/2) * W / nf * 0.29' pd='2*int((nf+1)/2) * (W / nf + 0.29)' ps='2*int((nf+2)/2) * (W / nf + 0.29)'
+ nrd='0.29 / W ' nrs='0.29 / W ' sa=0 sb=0 sd=0 mult=11 m=11
XMP2 comp bias1 VDD VDD sky130_fd_pr__pfet_01v8_lvt L=8 W='0.55 * 4 ' nf=4 ad='int((nf+1)/2) * W / nf * 0.29'
+ as='int((nf+2)/2) * W / nf * 0.29' pd='2*int((nf+1)/2) * (W / nf + 0.29)' ps='2*int((nf+2)/2) * (W / nf + 0.29)'
+ nrd='0.29 / W ' nrs='0.29 / W ' sa=0 sb=0 sd=0 mult=14 m=14
XMP3 net3 bias2 net4 VDD sky130_fd_pr__pfet_01v8_lvt L=1 W='3 * 3 ' nf=3 ad='int((nf+1)/2) * W / nf * 0.29'
+ as='int((nf+2)/2) * W / nf * 0.29' pd='2*int((nf+1)/2) * (W / nf + 0.29)' ps='2*int((nf+2)/2) * (W / nf + 0.29)'
+ nrd='0.29 / W ' nrs='0.29 / W ' sa=0 sb=0 sd=0 mult=11 m=11
XMP1 net4 bias1 VDD VDD sky130_fd_pr__pfet_01v8_lvt L=8 W='0.55 * 4 ' nf=4 ad='int((nf+1)/2) * W / nf * 0.29'
+ as='int((nf+2)/2) * W / nf * 0.29' pd='2*int((nf+1)/2) * (W / nf + 0.29)' ps='2*int((nf+2)/2) * (W / nf + 0.29)'
+ nrd='0.29 / W ' nrs='0.29 / W ' sa=0 sb=0 sd=0 mult=14 m=14
XMN5 net15 bias4 net8 VSS sky130_fd_pr__nfet_01v8 L=8 W='0.42 * 4 ' nf=4 ad='int((nf+1)/2) * W / nf * 0.29'
+ as='int((nf+2)/2) * W / nf * 0.29' pd='2*int((nf+1)/2) * (W / nf + 0.29)' ps='2*int((nf+2)/2) * (W / nf + 0.29)'
+ nrd='0.29 / W ' nrs='0.29 / W ' sa=0 sb=0 sd=0 mult=11 m=11
XMN1 net4 inn net5 VSS sky130_fd_pr__nfet_01v8_lvt L=0.5 W='1 * 5 ' nf=5 ad='int((nf+1)/2) * W / nf * 0.29'
+ as='int((nf+2)/2) * W / nf * 0.29' pd='2*int((nf+1)/2) * (W / nf + 0.29)' ps='2*int((nf+2)/2) * (W / nf + 0.29)'
+ nrd='0.29 / W ' nrs='0.29 / W ' sa=0 sb=0 sd=0 mult=1 m=1
XMN2 comp inp net5 VSS sky130_fd_pr__nfet_01v8_lvt L=0.5 W='1 * 5 ' nf=5 ad='int((nf+1)/2) * W / nf * 0.29'
+ as='int((nf+2)/2) * W / nf * 0.29' pd='2*int((nf+1)/2) * (W / nf + 0.29)' ps='2*int((nf+2)/2) * (W / nf + 0.29)'
+ nrd='0.29 / W ' nrs='0.29 / W ' sa=0 sb=0 sd=0 mult=1 m=1
XMN9 net7 net3 net9 VSS sky130_fd_pr__nfet_01v8 L=8 W='0.42 * 4 ' nf=4 ad='int((nf+1)/2) * W / nf * 0.29'
+ as='int((nf+2)/2) * W / nf * 0.29' pd='2*int((nf+1)/2) * (W / nf + 0.29)' ps='2*int((nf+2)/2) * (W / nf + 0.29)'
+ nrd='0.29 / W ' nrs='0.29 / W ' sa=0 sb=0 sd=0 mult=11 m=11
XMN10 net6 net3 net10 VSS sky130_fd_pr__nfet_01v8 L=8 W='0.42 * 4 ' nf=4 ad='int((nf+1)/2) * W / nf * 0.29'
+ as='int((nf+2)/2) * W / nf * 0.29' pd='2*int((nf+1)/2) * (W / nf + 0.29)' ps='2*int((nf+2)/2) * (W / nf + 0.29)'
+ nrd='0.29 / W ' nrs='0.29 / W ' sa=0 sb=0 sd=0 mult=11 m=11
XMN11 net8 bias4 net11 VSS sky130_fd_pr__nfet_01v8 L=8 W='0.42 * 4 ' nf=4 ad='int((nf+1)/2) * W / nf * 0.29'
+ as='int((nf+2)/2) * W / nf * 0.29' pd='2*int((nf+1)/2) * (W / nf + 0.29)' ps='2*int((nf+2)/2) * (W / nf + 0.29)'
+ nrd='0.29 / W ' nrs='0.29 / W ' sa=0 sb=0 sd=0 mult=11 m=11
XMN8 net9 net3 net12 VSS sky130_fd_pr__nfet_01v8 L=8 W='0.42 * 4 ' nf=4 ad='int((nf+1)/2) * W / nf * 0.29'
+ as='int((nf+2)/2) * W / nf * 0.29' pd='2*int((nf+1)/2) * (W / nf + 0.29)' ps='2*int((nf+2)/2) * (W / nf + 0.29)'
+ nrd='0.29 / W ' nrs='0.29 / W ' sa=0 sb=0 sd=0 mult=11 m=11
XMN12 net10 net3 net14 VSS sky130_fd_pr__nfet_01v8 L=8 W='0.42 * 4 ' nf=4 ad='int((nf+1)/2) * W / nf * 0.29'
+ as='int((nf+2)/2) * W / nf * 0.29' pd='2*int((nf+1)/2) * (W / nf + 0.29)' ps='2*int((nf+2)/2) * (W / nf + 0.29)'
+ nrd='0.29 / W ' nrs='0.29 / W ' sa=0 sb=0 sd=0 mult=11 m=11
XMN13 net11 bias4 net13 VSS sky130_fd_pr__nfet_01v8 L=8 W='0.42 * 4 ' nf=4 ad='int((nf+1)/2) * W / nf * 0.29'
+ as='int((nf+2)/2) * W / nf * 0.29' pd='2*int((nf+1)/2) * (W / nf + 0.29)' ps='2*int((nf+2)/2) * (W / nf + 0.29)'
+ nrd='0.29 / W ' nrs='0.29 / W ' sa=0 sb=0 sd=0 mult=11 m=11
XMN14 net12 net3 VSS VSS sky130_fd_pr__nfet_01v8 L=8 W='0.42 * 4 ' nf=4 ad='int((nf+1)/2) * W / nf * 0.29'
+ as='int((nf+2)/2) * W / nf * 0.29' pd='2*int((nf+1)/2) * (W / nf + 0.29)' ps='2*int((nf+2)/2) * (W / nf + 0.29)'
+ nrd='0.29 / W ' nrs='0.29 / W ' sa=0 sb=0 sd=0 mult=11 m=11
XMN15 net14 net3 VSS VSS sky130_fd_pr__nfet_01v8 L=8 W='0.42 * 4 ' nf=4 ad='int((nf+1)/2) * W / nf * 0.29'
+ as='int((nf+2)/2) * W / nf * 0.29' pd='2*int((nf+1)/2) * (W / nf + 0.29)' ps='2*int((nf+2)/2) * (W / nf + 0.29)'
+ nrd='0.29 / W ' nrs='0.29 / W ' sa=0 sb=0 sd=0 mult=11 m=11
XMN16 net13 bias4 VSS VSS sky130_fd_pr__nfet_01v8 L=8 W='0.42 * 4 ' nf=4 ad='int((nf+1)/2) * W / nf * 0.29'
+ as='int((nf+2)/2) * W / nf * 0.29' pd='2*int((nf+1)/2) * (W / nf + 0.29)' ps='2*int((nf+2)/2) * (W / nf + 0.29)'
+ nrd='0.29 / W ' nrs='0.29 / W ' sa=0 sb=0 sd=0 mult=11 m=11
XM9 net5 bias3 net15 VSS sky130_fd_pr__nfet_01v8_lvt L=0.5 W='1 * 2 ' nf=2 ad='int((nf+1)/2) * W / nf * 0.29'
+ as='int((nf+2)/2) * W / nf * 0.29' pd='2*int((nf+1)/2) * (W / nf + 0.29)' ps='2*int((nf+2)/2) * (W / nf + 0.29)'
+ nrd='0.29 / W ' nrs='0.29 / W ' sa=0 sb=0 sd=0 mult=11 m=11
.ends

.GLOBAL GND
.end
